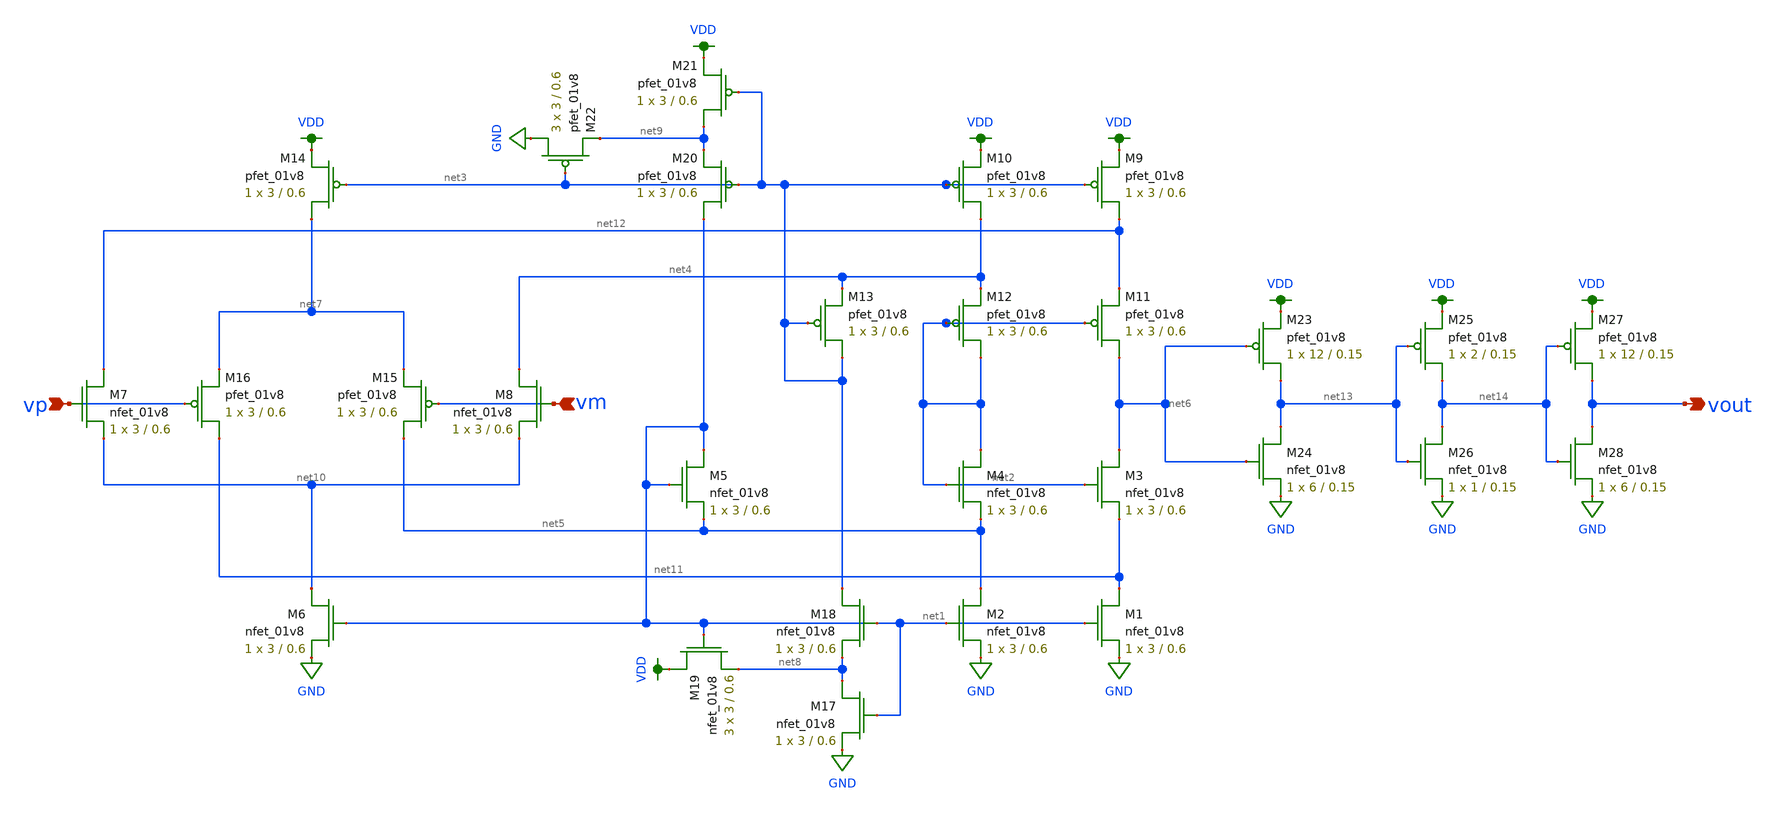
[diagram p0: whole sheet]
** sch_path: schematic/comparator_amp.sch
**.subckt comparator_amp vp vm vout
*.ipin vp
*.ipin vm
*.opin vout
XM1 net11 net1 GND GND sky130_fd_pr__nfet_01v8 L=0.6 W=3 nf=1 ad='int((nf+1)/2) * W/nf * 0.29' as='int((nf+2)/2) * W/nf * 0.29'
+ pd='2*int((nf+1)/2) * (W/nf + 0.29)' ps='2*int((nf+2)/2) * (W/nf + 0.29)' nrd='0.29 / W' nrs='0.29 / W'
+ sa=0 sb=0 sd=0 mult=1 m=1
XM9 net12 net3 VDD VDD sky130_fd_pr__pfet_01v8 L=0.6 W=3 nf=1 ad='int((nf+1)/2) * W/nf * 0.29' as='int((nf+2)/2) * W/nf * 0.29'
+ pd='2*int((nf+1)/2) * (W/nf + 0.29)' ps='2*int((nf+2)/2) * (W/nf + 0.29)' nrd='0.29 / W' nrs='0.29 / W'
+ sa=0 sb=0 sd=0 mult=1 m=1
XM2 net5 net1 GND GND sky130_fd_pr__nfet_01v8 L=0.6 W=3 nf=1 ad='int((nf+1)/2) * W/nf * 0.29' as='int((nf+2)/2) * W/nf * 0.29'
+ pd='2*int((nf+1)/2) * (W/nf + 0.29)' ps='2*int((nf+2)/2) * (W/nf + 0.29)' nrd='0.29 / W' nrs='0.29 / W'
+ sa=0 sb=0 sd=0 mult=1 m=1
XM3 net6 net2 net11 GND sky130_fd_pr__nfet_01v8 L=0.6 W=3 nf=1 ad='int((nf+1)/2) * W/nf * 0.29' as='int((nf+2)/2) * W/nf * 0.29'
+ pd='2*int((nf+1)/2) * (W/nf + 0.29)' ps='2*int((nf+2)/2) * (W/nf + 0.29)' nrd='0.29 / W' nrs='0.29 / W'
+ sa=0 sb=0 sd=0 mult=1 m=1
XM4 net2 net2 net5 GND sky130_fd_pr__nfet_01v8 L=0.6 W=3 nf=1 ad='int((nf+1)/2) * W/nf * 0.29' as='int((nf+2)/2) * W/nf * 0.29'
+ pd='2*int((nf+1)/2) * (W/nf + 0.29)' ps='2*int((nf+2)/2) * (W/nf + 0.29)' nrd='0.29 / W' nrs='0.29 / W'
+ sa=0 sb=0 sd=0 mult=1 m=1
XM5 net1 net1 net5 GND sky130_fd_pr__nfet_01v8 L=0.6 W=3 nf=1 ad='int((nf+1)/2) * W/nf * 0.29' as='int((nf+2)/2) * W/nf * 0.29'
+ pd='2*int((nf+1)/2) * (W/nf + 0.29)' ps='2*int((nf+2)/2) * (W/nf + 0.29)' nrd='0.29 / W' nrs='0.29 / W'
+ sa=0 sb=0 sd=0 mult=1 m=1
XM6 net10 net1 GND GND sky130_fd_pr__nfet_01v8 L=0.6 W=3 nf=1 ad='int((nf+1)/2) * W/nf * 0.29' as='int((nf+2)/2) * W/nf * 0.29'
+ pd='2*int((nf+1)/2) * (W/nf + 0.29)' ps='2*int((nf+2)/2) * (W/nf + 0.29)' nrd='0.29 / W' nrs='0.29 / W'
+ sa=0 sb=0 sd=0 mult=1 m=1
XM7 net12 vp net10 GND sky130_fd_pr__nfet_01v8 L=0.6 W=3 nf=1 ad='int((nf+1)/2) * W/nf * 0.29' as='int((nf+2)/2) * W/nf * 0.29'
+ pd='2*int((nf+1)/2) * (W/nf + 0.29)' ps='2*int((nf+2)/2) * (W/nf + 0.29)' nrd='0.29 / W' nrs='0.29 / W'
+ sa=0 sb=0 sd=0 mult=1 m=1
XM8 net4 vm net10 GND sky130_fd_pr__nfet_01v8 L=0.6 W=3 nf=1 ad='int((nf+1)/2) * W/nf * 0.29' as='int((nf+2)/2) * W/nf * 0.29'
+ pd='2*int((nf+1)/2) * (W/nf + 0.29)' ps='2*int((nf+2)/2) * (W/nf + 0.29)' nrd='0.29 / W' nrs='0.29 / W'
+ sa=0 sb=0 sd=0 mult=1 m=1
XM10 net4 net3 VDD VDD sky130_fd_pr__pfet_01v8 L=0.6 W=3 nf=1 ad='int((nf+1)/2) * W/nf * 0.29' as='int((nf+2)/2) * W/nf * 0.29'
+ pd='2*int((nf+1)/2) * (W/nf + 0.29)' ps='2*int((nf+2)/2) * (W/nf + 0.29)' nrd='0.29 / W' nrs='0.29 / W'
+ sa=0 sb=0 sd=0 mult=1 m=1
XM11 net6 net2 net12 VDD sky130_fd_pr__pfet_01v8 L=0.6 W=3 nf=1 ad='int((nf+1)/2) * W/nf * 0.29' as='int((nf+2)/2) * W/nf * 0.29'
+ pd='2*int((nf+1)/2) * (W/nf + 0.29)' ps='2*int((nf+2)/2) * (W/nf + 0.29)' nrd='0.29 / W' nrs='0.29 / W'
+ sa=0 sb=0 sd=0 mult=1 m=1
XM12 net2 net2 net4 VDD sky130_fd_pr__pfet_01v8 L=0.6 W=3 nf=1 ad='int((nf+1)/2) * W/nf * 0.29' as='int((nf+2)/2) * W/nf * 0.29'
+ pd='2*int((nf+1)/2) * (W/nf + 0.29)' ps='2*int((nf+2)/2) * (W/nf + 0.29)' nrd='0.29 / W' nrs='0.29 / W'
+ sa=0 sb=0 sd=0 mult=1 m=1
XM13 net3 net3 net4 VDD sky130_fd_pr__pfet_01v8 L=0.6 W=3 nf=1 ad='int((nf+1)/2) * W/nf * 0.29' as='int((nf+2)/2) * W/nf * 0.29'
+ pd='2*int((nf+1)/2) * (W/nf + 0.29)' ps='2*int((nf+2)/2) * (W/nf + 0.29)' nrd='0.29 / W' nrs='0.29 / W'
+ sa=0 sb=0 sd=0 mult=1 m=1
XM14 net7 net3 VDD VDD sky130_fd_pr__pfet_01v8 L=0.6 W=3 nf=1 ad='int((nf+1)/2) * W/nf * 0.29' as='int((nf+2)/2) * W/nf * 0.29'
+ pd='2*int((nf+1)/2) * (W/nf + 0.29)' ps='2*int((nf+2)/2) * (W/nf + 0.29)' nrd='0.29 / W' nrs='0.29 / W'
+ sa=0 sb=0 sd=0 mult=1 m=1
XM15 net5 vm net7 VDD sky130_fd_pr__pfet_01v8 L=0.6 W=3 nf=1 ad='int((nf+1)/2) * W/nf * 0.29' as='int((nf+2)/2) * W/nf * 0.29'
+ pd='2*int((nf+1)/2) * (W/nf + 0.29)' ps='2*int((nf+2)/2) * (W/nf + 0.29)' nrd='0.29 / W' nrs='0.29 / W'
+ sa=0 sb=0 sd=0 mult=1 m=1
XM16 net11 vp net7 VDD sky130_fd_pr__pfet_01v8 L=0.6 W=3 nf=1 ad='int((nf+1)/2) * W/nf * 0.29' as='int((nf+2)/2) * W/nf * 0.29'
+ pd='2*int((nf+1)/2) * (W/nf + 0.29)' ps='2*int((nf+2)/2) * (W/nf + 0.29)' nrd='0.29 / W' nrs='0.29 / W'
+ sa=0 sb=0 sd=0 mult=1 m=1
XM17 net8 net1 GND GND sky130_fd_pr__nfet_01v8 L=0.6 W=3 nf=1 ad='int((nf+1)/2) * W/nf * 0.29' as='int((nf+2)/2) * W/nf * 0.29'
+ pd='2*int((nf+1)/2) * (W/nf + 0.29)' ps='2*int((nf+2)/2) * (W/nf + 0.29)' nrd='0.29 / W' nrs='0.29 / W'
+ sa=0 sb=0 sd=0 mult=1 m=1
XM18 net3 net1 net8 GND sky130_fd_pr__nfet_01v8 L=0.6 W=3 nf=1 ad='int((nf+1)/2) * W/nf * 0.29' as='int((nf+2)/2) * W/nf * 0.29'
+ pd='2*int((nf+1)/2) * (W/nf + 0.29)' ps='2*int((nf+2)/2) * (W/nf + 0.29)' nrd='0.29 / W' nrs='0.29 / W'
+ sa=0 sb=0 sd=0 mult=1 m=1
XM19 VDD net1 net8 GND sky130_fd_pr__nfet_01v8 L=0.6 W=3 nf=1 ad='int((nf+1)/2) * W/nf * 0.29' as='int((nf+2)/2) * W/nf * 0.29'
+ pd='2*int((nf+1)/2) * (W/nf + 0.29)' ps='2*int((nf+2)/2) * (W/nf + 0.29)' nrd='0.29 / W' nrs='0.29 / W'
+ sa=0 sb=0 sd=0 mult=3 m=3
XM20 net1 net3 net9 VDD sky130_fd_pr__pfet_01v8 L=0.6 W=3 nf=1 ad='int((nf+1)/2) * W/nf * 0.29' as='int((nf+2)/2) * W/nf * 0.29'
+ pd='2*int((nf+1)/2) * (W/nf + 0.29)' ps='2*int((nf+2)/2) * (W/nf + 0.29)' nrd='0.29 / W' nrs='0.29 / W'
+ sa=0 sb=0 sd=0 mult=1 m=1
XM21 net9 net3 VDD VDD sky130_fd_pr__pfet_01v8 L=0.6 W=3 nf=1 ad='int((nf+1)/2) * W/nf * 0.29' as='int((nf+2)/2) * W/nf * 0.29'
+ pd='2*int((nf+1)/2) * (W/nf + 0.29)' ps='2*int((nf+2)/2) * (W/nf + 0.29)' nrd='0.29 / W' nrs='0.29 / W'
+ sa=0 sb=0 sd=0 mult=1 m=1
XM22 GND net3 net9 VDD sky130_fd_pr__pfet_01v8 L=0.6 W=3 nf=1 ad='int((nf+1)/2) * W/nf * 0.29' as='int((nf+2)/2) * W/nf * 0.29'
+ pd='2*int((nf+1)/2) * (W/nf + 0.29)' ps='2*int((nf+2)/2) * (W/nf + 0.29)' nrd='0.29 / W' nrs='0.29 / W'
+ sa=0 sb=0 sd=0 mult=3 m=3
XM23 net13 net6 VDD VDD sky130_fd_pr__pfet_01v8 L=0.15 W=12 nf=1 ad='int((nf+1)/2) * W/nf * 0.29' as='int((nf+2)/2) * W/nf * 0.29'
+ pd='2*int((nf+1)/2) * (W/nf + 0.29)' ps='2*int((nf+2)/2) * (W/nf + 0.29)' nrd='0.29 / W' nrs='0.29 / W'
+ sa=0 sb=0 sd=0 mult=1 m=1
XM24 net13 net6 GND GND sky130_fd_pr__nfet_01v8 L=0.15 W=6 nf=1 ad='int((nf+1)/2) * W/nf * 0.29' as='int((nf+2)/2) * W/nf * 0.29'
+ pd='2*int((nf+1)/2) * (W/nf + 0.29)' ps='2*int((nf+2)/2) * (W/nf + 0.29)' nrd='0.29 / W' nrs='0.29 / W'
+ sa=0 sb=0 sd=0 mult=1 m=1
XM25 net14 net13 VDD VDD sky130_fd_pr__pfet_01v8 L=0.15 W=2 nf=1 ad='int((nf+1)/2) * W/nf * 0.29' as='int((nf+2)/2) * W/nf * 0.29'
+ pd='2*int((nf+1)/2) * (W/nf + 0.29)' ps='2*int((nf+2)/2) * (W/nf + 0.29)' nrd='0.29 / W' nrs='0.29 / W'
+ sa=0 sb=0 sd=0 mult=1 m=1
XM26 net14 net13 GND GND sky130_fd_pr__nfet_01v8 L=0.15 W=1 nf=1 ad='int((nf+1)/2) * W/nf * 0.29' as='int((nf+2)/2) * W/nf * 0.29'
+ pd='2*int((nf+1)/2) * (W/nf + 0.29)' ps='2*int((nf+2)/2) * (W/nf + 0.29)' nrd='0.29 / W' nrs='0.29 / W'
+ sa=0 sb=0 sd=0 mult=1 m=1
XM27 vout net14 VDD VDD sky130_fd_pr__pfet_01v8 L=0.15 W=12 nf=1 ad='int((nf+1)/2) * W/nf * 0.29' as='int((nf+2)/2) * W/nf * 0.29'
+ pd='2*int((nf+1)/2) * (W/nf + 0.29)' ps='2*int((nf+2)/2) * (W/nf + 0.29)' nrd='0.29 / W' nrs='0.29 / W'
+ sa=0 sb=0 sd=0 mult=1 m=1
XM28 vout net14 GND GND sky130_fd_pr__nfet_01v8 L=0.15 W=6 nf=1 ad='int((nf+1)/2) * W/nf * 0.29' as='int((nf+2)/2) * W/nf * 0.29'
+ pd='2*int((nf+1)/2) * (W/nf + 0.29)' ps='2*int((nf+2)/2) * (W/nf + 0.29)' nrd='0.29 / W' nrs='0.29 / W'
+ sa=0 sb=0 sd=0 mult=1 m=1
**.ends
.GLOBAL GND
.GLOBAL VDD
.end
